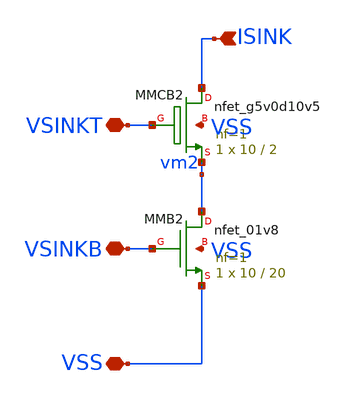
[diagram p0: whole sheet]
** sch_path: tt08/ip/vthref_tt/xschem/vthref_sink.sch
**.subckt vthref_sink VSS ISINK VSINKT VSINKB
*.iopin VSS
*.ipin ISINK
*.iopin VSINKT
*.iopin VSINKB
XMMCB2 ISINK VSINKT vm2 VSS sky130_fd_pr__nfet_g5v0d10v5 L=2 W=10 nf=1 ad='int((nf+1)/2) * W/nf * 0.29'
+ as='int((nf+2)/2) * W/nf * 0.29' pd='2*int((nf+1)/2) * (W/nf + 0.29)' ps='2*int((nf+2)/2) * (W/nf + 0.29)'
+ nrd='0.29 / W' nrs='0.29 / W' sa=0 sb=0 sd=0 mult=1 m=1
XMMB2 vm2 VSINKB VSS VSS sky130_fd_pr__nfet_01v8 L=20 W=10 nf=1 ad='int((nf+1)/2) * W/nf * 0.29' as='int((nf+2)/2) * W/nf * 0.29'
+ pd='2*int((nf+1)/2) * (W/nf + 0.29)' ps='2*int((nf+2)/2) * (W/nf + 0.29)' nrd='0.29 / W' nrs='0.29 / W'
+ sa=0 sb=0 sd=0 mult=1 m=1
**.ends
.end
